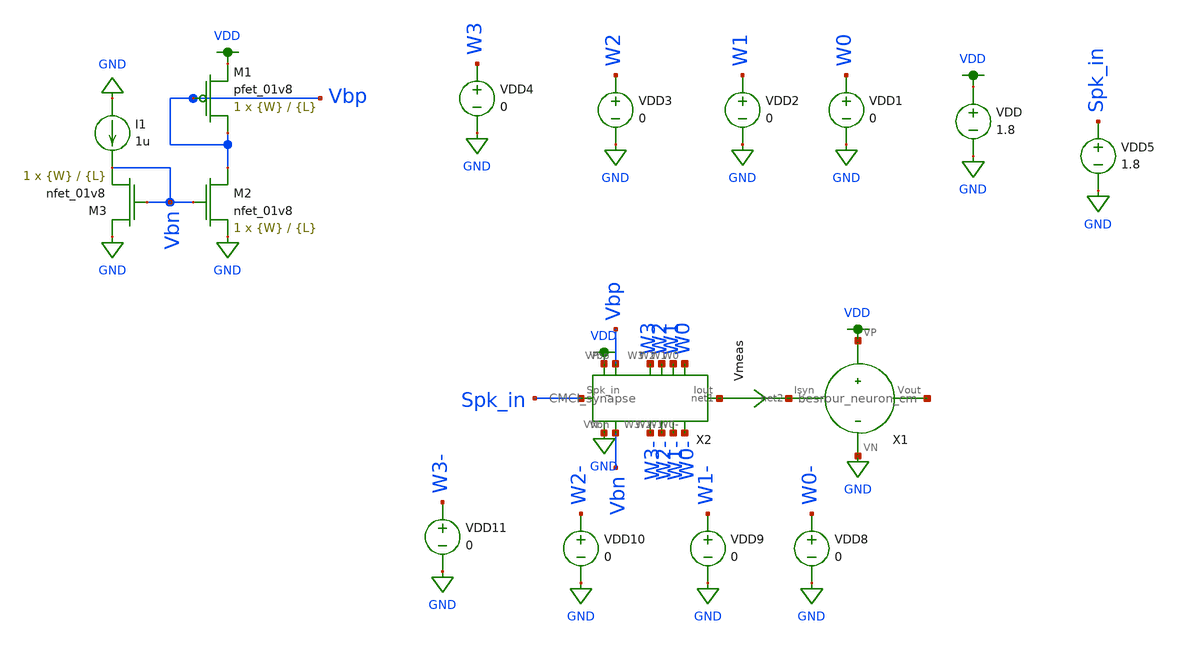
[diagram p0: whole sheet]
** sch_path: schematic/tran_CMCI.sch
**.subckt tran_CMCI
VDD VDD GND 1.8
VDD1 W0 GND 0
VDD2 W1 GND 0
VDD3 W2 GND 0
VDD4 W3 GND 0
VDD5 Spk_in GND 1.8
VDD8 W0- GND 0
VDD9 W1- GND 0
VDD10 W2- GND 0
VDD11 W3- GND 0
Vmeas net1 net2 0
.save i(vmeas)
XM1 Vbp Vbp VDD VDD sky130_fd_pr__pfet_01v8 L={L} W={W} nf=1 ad='int((nf+1)/2) * W/nf * 0.29' as='int((nf+2)/2) * W/nf * 0.29'
+ pd='2*int((nf+1)/2) * (W/nf + 0.29)' ps='2*int((nf+2)/2) * (W/nf + 0.29)' nrd='0.29 / W' nrs='0.29 / W'
+ sa=0 sb=0 sd=0 mult=1 m=1
XM2 Vbp Vbn GND GND sky130_fd_pr__nfet_01v8 L={L} W={W} nf=1 ad='int((nf+1)/2) * W/nf * 0.29' as='int((nf+2)/2) * W/nf * 0.29'
+ pd='2*int((nf+1)/2) * (W/nf + 0.29)' ps='2*int((nf+2)/2) * (W/nf + 0.29)' nrd='0.29 / W' nrs='0.29 / W'
+ sa=0 sb=0 sd=0 mult=1 m=1
XM3 GND Vbn Vbn GND sky130_fd_pr__nfet_01v8 L={L} W={W} nf=1 ad='int((nf+1)/2) * W/nf * 0.29' as='int((nf+2)/2) * W/nf * 0.29'
+ pd='2*int((nf+1)/2) * (W/nf + 0.29)' ps='2*int((nf+2)/2) * (W/nf + 0.29)' nrd='0.29 / W' nrs='0.29 / W'
+ sa=0 sb=0 sd=0 mult=1 m=1
I1 GND Vbn 1u
X1 net2 net3 VDD GND besrour_neuron_cm
X2 VDD Vbp W3 W2 W1 W0 net1 W0- W1- W2- W3- Vbn GND Spk_in CMCI_synapse
**** begin user architecture code

.param W=12
.param L=0.5
.control
set wr_vecnames
set wr_singlescale
let code = 0
  while code < 16
    if code eq 0
      let W0- = 0
    else
      let W0- = code % 2 * 1.8
    end
    if floor(code / 2) eq 0
      let W1- = 0
    else
      let W1- = floor(code / 2) % 2 * 1.8
    end
    if floor(code / 4) eq 0
      let W2- = 0
    else
      let W2- = floor(code / 4) % 2 * 1.8
    end
    if floor(code / 8) eq 0
      let W3- = 0
    else
      let W3- = floor(code / 8) % 2 * 1.8
    end
    alter vdd8 $&w0-
    alter vdd9 $&w1-
    alter vdd10 $&w2-
    alter vdd11 $&w3-
    save all
    op
    wrdata ~/neuromorphic_computing_final/dac_sim.txt i(Vmeas) v(W3-) v(W2-) v(W1-) v(W0-)
    if code eq 0
      set appendwrite
      set wr_vecnames = FALSE
    end
    let code = code + 1
  end
.endc


.option wnflag=1
.param MC_SWITCH=0.0
.lib ~/skywater/skywater-pdk/libraries/sky130_fd_pr_ngspice/latest/models/sky130.lib.spice tt

**** end user architecture code
**.ends
.GLOBAL VDD
.GLOBAL GND
.end
